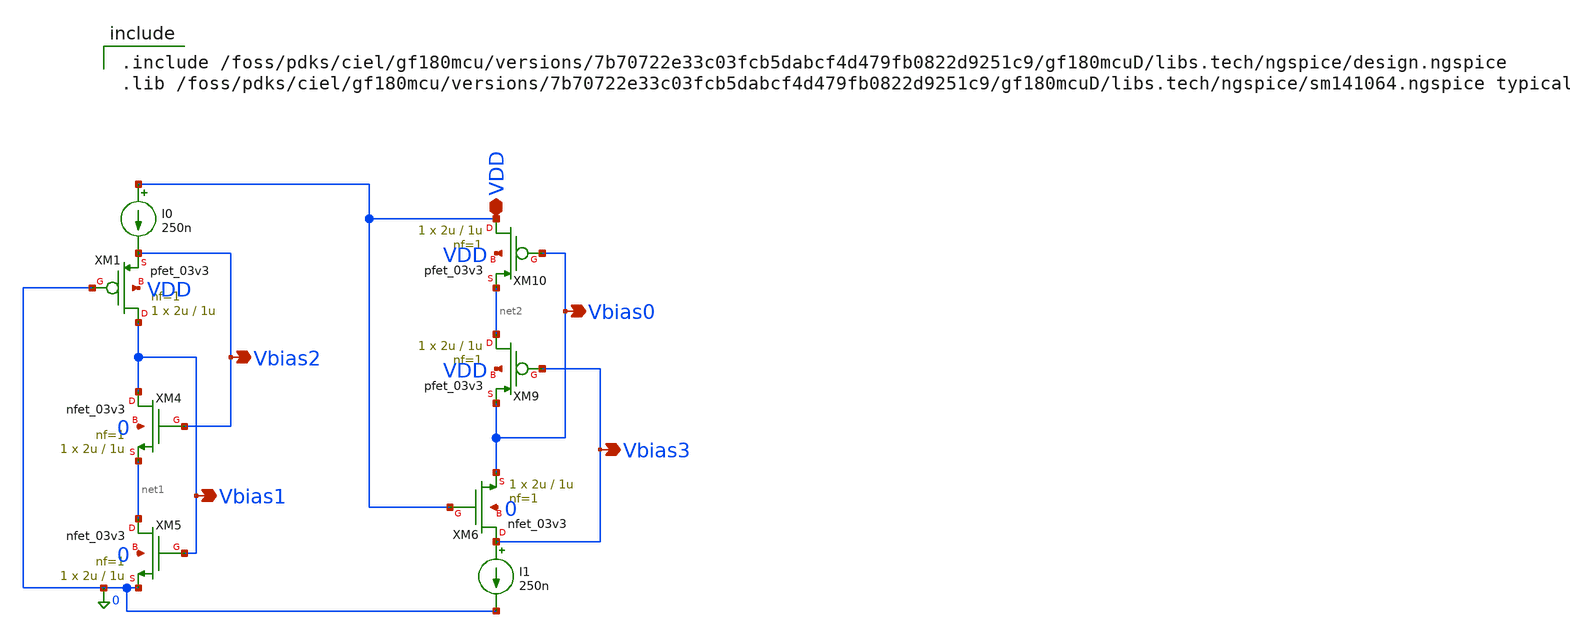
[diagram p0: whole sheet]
** sch_path: analog/B04_OTA_bias_bpf_fc.sch
**.subckt B04_OTA_bias_bpf_fc VDD Vbias2 Vbias1 Vbias0 Vbias3
*.iopin VDD
*.opin Vbias2
*.opin Vbias1
*.opin Vbias0
*.opin Vbias3
XM1 Vbias1 0 Vbias2 VDD pfet_03v3 L=1u W=2u nf=1 ad='int((nf+1)/2) * W/nf * 0.18u' as='int((nf+2)/2) * W/nf * 0.18u'
+ pd='2*int((nf+1)/2) * (W/nf + 0.18u)' ps='2*int((nf+2)/2) * (W/nf + 0.18u)' nrd='0.18u / W' nrs='0.18u / W'
+ sa=0 sb=0 sd=0 m=1
XM4 Vbias1 Vbias2 net1 0 nfet_03v3 L=1u W=2u nf=1 ad='int((nf+1)/2) * W/nf * 0.18u' as='int((nf+2)/2) * W/nf * 0.18u'
+ pd='2*int((nf+1)/2) * (W/nf + 0.18u)' ps='2*int((nf+2)/2) * (W/nf + 0.18u)' nrd='0.18u / W' nrs='0.18u / W'
+ sa=0 sb=0 sd=0 m=1
XM5 net1 Vbias1 0 0 nfet_03v3 L=1u W=2u nf=1 ad='int((nf+1)/2) * W/nf * 0.18u' as='int((nf+2)/2) * W/nf * 0.18u'
+ pd='2*int((nf+1)/2) * (W/nf + 0.18u)' ps='2*int((nf+2)/2) * (W/nf + 0.18u)' nrd='0.18u / W' nrs='0.18u / W'
+ sa=0 sb=0 sd=0 m=1
XM9 net2 Vbias3 Vbias0 VDD pfet_03v3 L=1u W=2u nf=1 ad='int((nf+1)/2) * W/nf * 0.18u' as='int((nf+2)/2) * W/nf * 0.18u'
+ pd='2*int((nf+1)/2) * (W/nf + 0.18u)' ps='2*int((nf+2)/2) * (W/nf + 0.18u)' nrd='0.18u / W' nrs='0.18u / W'
+ sa=0 sb=0 sd=0 m=1
XM10 VDD Vbias0 net2 VDD pfet_03v3 L=1u W=2u nf=1 ad='int((nf+1)/2) * W/nf * 0.18u' as='int((nf+2)/2) * W/nf * 0.18u'
+ pd='2*int((nf+1)/2) * (W/nf + 0.18u)' ps='2*int((nf+2)/2) * (W/nf + 0.18u)' nrd='0.18u / W' nrs='0.18u / W'
+ sa=0 sb=0 sd=0 m=1
XM6 Vbias3 VDD Vbias0 0 nfet_03v3 L=1u W=2u nf=1 ad='int((nf+1)/2) * W/nf * 0.18u' as='int((nf+2)/2) * W/nf * 0.18u'
+ pd='2*int((nf+1)/2) * (W/nf + 0.18u)' ps='2*int((nf+2)/2) * (W/nf + 0.18u)' nrd='0.18u / W' nrs='0.18u / W'
+ sa=0 sb=0 sd=0 m=1
I0 VDD Vbias2 250n
I1 Vbias3 0 250n
**** begin user architecture code

.include /foss/pdks/ciel/gf180mcu/versions/7b70722e33c03fcb5dabcf4d479fb0822d9251c9/gf180mcuD/libs.tech/ngspice/design.ngspice
.lib /foss/pdks/ciel/gf180mcu/versions/7b70722e33c03fcb5dabcf4d479fb0822d9251c9/gf180mcuD/libs.tech/ngspice/sm141064.ngspice typical

**** end user architecture code
**.ends
.end
